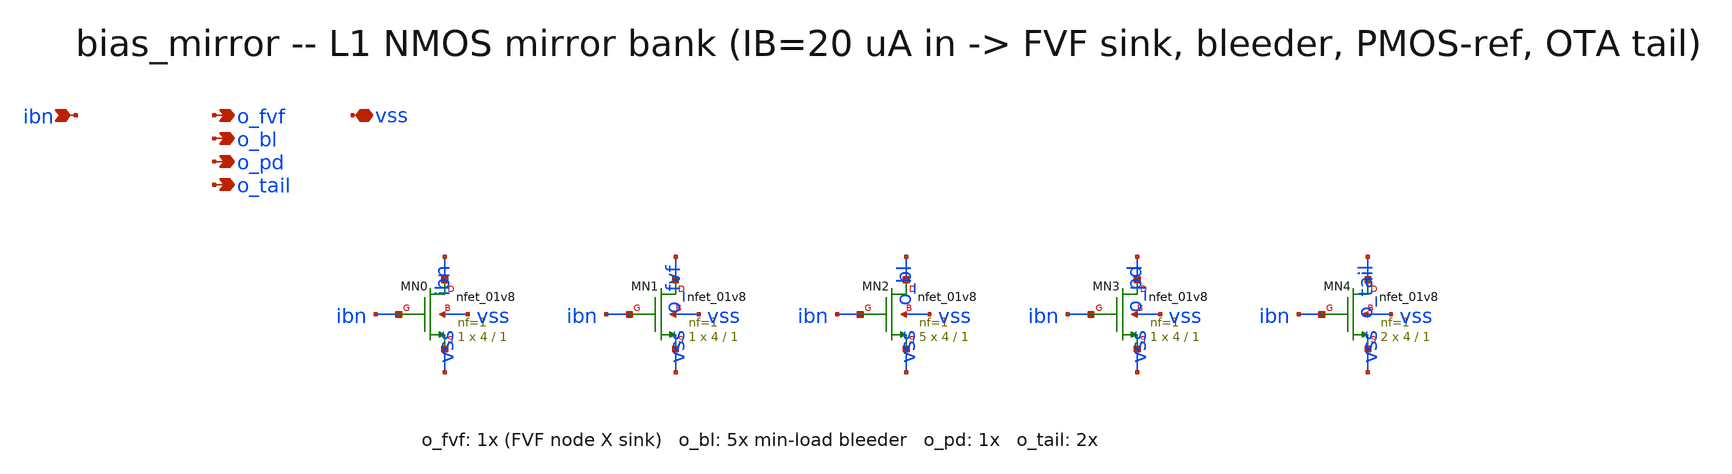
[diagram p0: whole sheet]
** sch_path: xschem/onetops/bias_mirror.sch
**.subckt bias_mirror ibn o_fvf o_bl o_pd o_tail vss
*.ipin ibn
*.opin o_fvf
*.opin o_bl
*.opin o_pd
*.opin o_tail
*.iopin vss
XMN0 ibn ibn vss vss sky130_fd_pr__nfet_01v8 L=1 W=4 nf=1 ad='int((1 + 1)/2) * 4 / 1 * 0.29' as='int((1 + 2)/2) * 4 / 1 * 0.29'
+ pd='2*int((1 + 1)/2) * (4 / 1 + 0.29)' ps='2*int((1 + 2)/2) * (4 / 1 + 0.29)' nrd='0.29 / 4 ' nrs='0.29 / 4 '
+ sa=0 sb=0 sd=0 mult=1 m=1
XMN1 o_fvf ibn vss vss sky130_fd_pr__nfet_01v8 L=1 W=4 nf=1 ad='int((1 + 1)/2) * 4 / 1 * 0.29' as='int((1 + 2)/2) * 4 / 1 * 0.29'
+ pd='2*int((1 + 1)/2) * (4 / 1 + 0.29)' ps='2*int((1 + 2)/2) * (4 / 1 + 0.29)' nrd='0.29 / 4 ' nrs='0.29 / 4 '
+ sa=0 sb=0 sd=0 mult=1 m=1
XMN2 o_bl ibn vss vss sky130_fd_pr__nfet_01v8 L=1 W=4 nf=1 ad='int((1 + 1)/2) * 4 / 1 * 0.29' as='int((1 + 2)/2) * 4 / 1 * 0.29'
+ pd='2*int((1 + 1)/2) * (4 / 1 + 0.29)' ps='2*int((1 + 2)/2) * (4 / 1 + 0.29)' nrd='0.29 / 4 ' nrs='0.29 / 4 '
+ sa=0 sb=0 sd=0 mult=5 m=5
XMN3 o_pd ibn vss vss sky130_fd_pr__nfet_01v8 L=1 W=4 nf=1 ad='int((1 + 1)/2) * 4 / 1 * 0.29' as='int((1 + 2)/2) * 4 / 1 * 0.29'
+ pd='2*int((1 + 1)/2) * (4 / 1 + 0.29)' ps='2*int((1 + 2)/2) * (4 / 1 + 0.29)' nrd='0.29 / 4 ' nrs='0.29 / 4 '
+ sa=0 sb=0 sd=0 mult=1 m=1
XMN4 o_tail ibn vss vss sky130_fd_pr__nfet_01v8 L=1 W=4 nf=1 ad='int((1 + 1)/2) * 4 / 1 * 0.29' as='int((1 + 2)/2) * 4 / 1 * 0.29'
+ pd='2*int((1 + 1)/2) * (4 / 1 + 0.29)' ps='2*int((1 + 2)/2) * (4 / 1 + 0.29)' nrd='0.29 / 4 ' nrs='0.29 / 4 '
+ sa=0 sb=0 sd=0 mult=2 m=2
**.ends
.end
